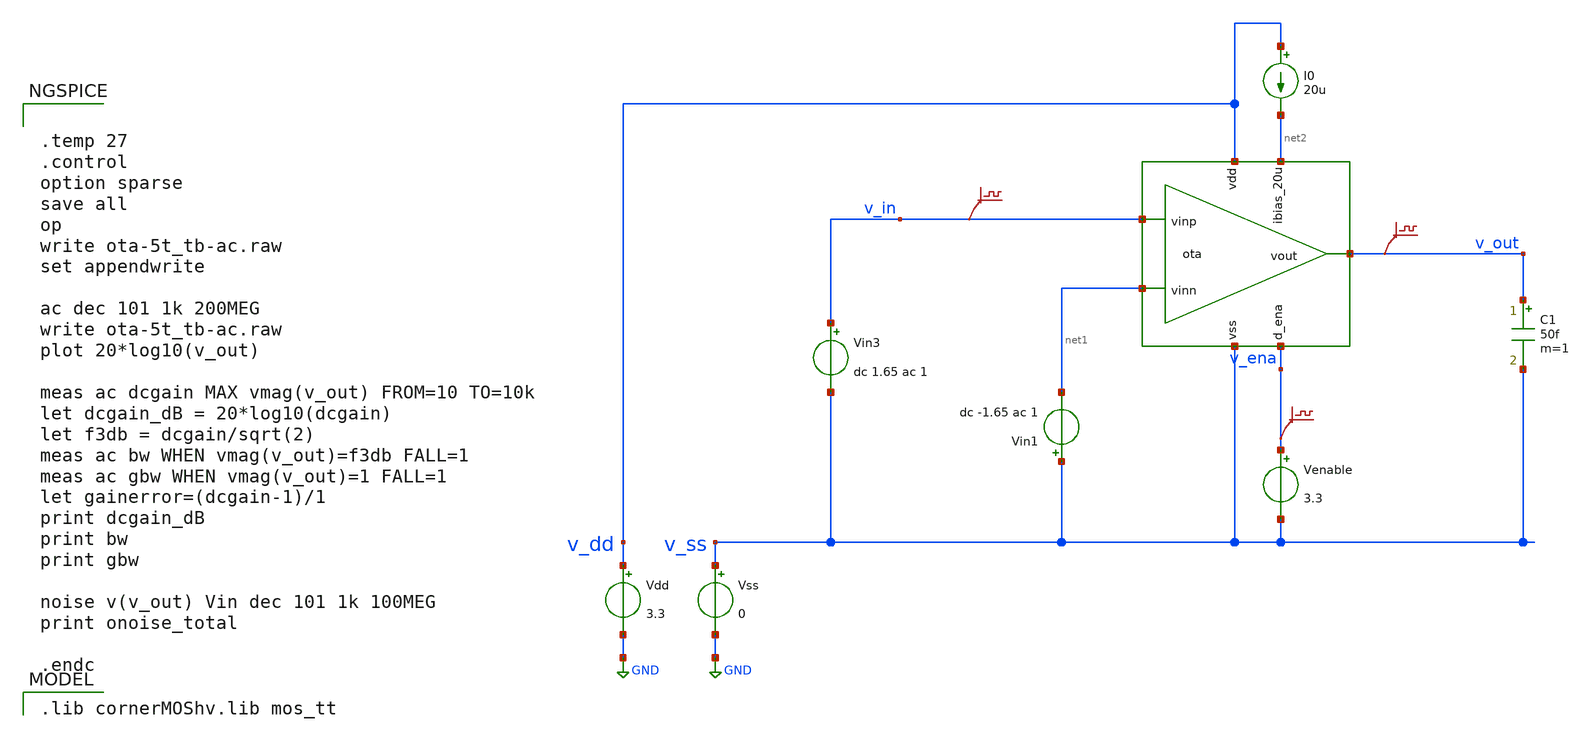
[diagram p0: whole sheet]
** sch_path: Differntial_Amp/design_data/xschem/ota-5t_tb-ac.sch
* Copyright 2024 Harald Pretl
**.subckt ota-5t_tb-ac
Vdd v_dd GND 3.3
Vss v_ss GND 0
C1 v_out v_ss 50f m=1
I0 v_dd net2 20u
Venable v_ena v_ss 3.3
.save v(v_in)
.save v(v_out)
.save v(v_ena)
x1 v_dd v_out v_in net1 net2 v_ss v_ena ota
Vin1 v_ss net1 dc -1.65 ac 1
Vin3 v_in v_ss dc 1.65 ac 1
**** begin user architecture code
 .lib cornerMOShv.lib mos_tt



.temp 27
.control
option sparse
save all
op
write ota-5t_tb-ac.raw
set appendwrite

ac dec 101 1k 200MEG
write ota-5t_tb-ac.raw
plot 20*log10(v_out)

meas ac dcgain MAX vmag(v_out) FROM=10 TO=10k
let dcgain_dB = 20*log10(dcgain)
let f3db = dcgain/sqrt(2)
meas ac bw WHEN vmag(v_out)=f3db FALL=1
meas ac gbw WHEN vmag(v_out)=1 FALL=1
let gainerror=(dcgain-1)/1
print dcgain_dB
print bw
print gbw

noise v(v_out) Vin dec 101 1k 100MEG
print onoise_total

.endc


**** end user architecture code
**.ends

* expanding   symbol:
*+  /home/aidas93/Downloads/TO_Nov2024-main/Differntial_Amp/design_data/xschem/ota.sym # of pins=7
** sym_path: Differntial_Amp/design_data/xschem/ota.sym
** sch_path: Differntial_Amp/design_data/xschem/ota.sch
.subckt ota vdd vout vinp vinn ibias_20u vss d_ena
*.opin vout
*.iopin vdd
*.iopin vss
*.ipin ibias_20u
*.ipin vinn
*.ipin vinp
*.ipin d_ena
XM1 vout vinn net2 vss sg13_hv_nmos w=0.53u l=1u ng=1 m=4 mm_ok=1
XM2 net1 vinp net2 vss sg13_hv_nmos w=0.53u l=1u ng=1 m=4 mm_ok=1
XM5 net2 net3 vss vss sg13_hv_nmos w=0.76u l=1u ng=1 m=1 mm_ok=1
XM3 net1 net1 vdd vdd sg13_hv_pmos w=1.45u l=1u ng=1 m=1 mm_ok=1
XM4 vout net1 vdd vdd sg13_hv_pmos w=1.45u l=1u ng=1 m=1 mm_ok=1
XM6 ibias_20u net3 vss vss sg13_hv_nmos w=3.075u l=1u ng=5 m=1 mm_ok=1
XM7 net1 d_ena vdd vdd sg13_hv_pmos w=1.5u l=1u ng=1 m=1 mm_ok=1
XM8 net4 d_ena vdd vdd sg13_hv_pmos w=1.5u l=1u ng=1 m=1 mm_ok=1
XM9 ibias_20u net4 net3 vss sg13_hv_nmos w=0.5u l=1u ng=1 m=1 mm_ok=1
XM10 net3 net4 vss vss sg13_hv_nmos w=0.5u l=1u ng=1 m=1 mm_ok=1
XM11 net4 d_ena vss vss sg13_hv_nmos w=0.5u l=1u ng=1 m=1 mm_ok=1
XM12 vss vss vss vss sg13_hv_nmos w=0.5u l=0.5u ng=1 m=1 mm_ok=1
XM13 vss vss vss vss sg13_hv_nmos w=0.5u l=0.5u ng=1 m=1 mm_ok=1
XM14 vss vss vss vss sg13_hv_nmos w=0.76u l=0.5u ng=1 m=1 mm_ok=1
XM15 vss vss vss vss sg13_hv_nmos w=0.615u l=0.5u ng=1 m=1 mm_ok=1
XM16 vss vss vss vss sg13_hv_nmos w=0.615u l=0.5u ng=1 m=1 mm_ok=1
XM17 vss vss vss vss sg13_hv_nmos w=0.76u l=0.5u ng=1 m=1 mm_ok=1
XM18 vss vss vss vss sg13_hv_nmos w=0.5u l=0.5u ng=1 m=1 mm_ok=1
XM19 vss vss vss vss sg13_hv_nmos w=0.5u l=0.5u ng=1 m=1 mm_ok=1
XM20 vss vss vss vss sg13_hv_nmos w=0.53u l=0.5u ng=1 m=1 mm_ok=1
XM21 vss vss vss vss sg13_hv_nmos w=0.53u l=0.5u ng=1 m=1 mm_ok=1
XM22 vss vss vss vss sg13_hv_nmos w=0.53u l=0.5u ng=1 m=1 mm_ok=1
XM23 vss vss vss vss sg13_hv_nmos w=0.53u l=0.5u ng=1 m=1 mm_ok=1
XM24 vss vss vss vss sg13_hv_nmos w=0.5u l=1u ng=1 m=1 mm_ok=1
XM25 vss vss vss vss sg13_hv_nmos w=0.5u l=1u ng=1 m=1 mm_ok=1
XM26 vss vss vss vss sg13_hv_nmos w=0.5u l=0.5u ng=1 m=1 mm_ok=1
XM27 vss vss vss vss sg13_hv_nmos w=0.5u l=0.5u ng=1 m=1 mm_ok=1
XM28 vss vss vss vss sg13_hv_nmos w=0.53u l=0.5u ng=1 m=1 mm_ok=1
XM29 vss vss vss vss sg13_hv_nmos w=0.53u l=0.5u ng=1 m=1 mm_ok=1
XM30 vss vss vss vss sg13_hv_nmos w=0.53u l=0.5u ng=1 m=1 mm_ok=1
XM31 vss vss vss vss sg13_hv_nmos w=0.53u l=0.5u ng=1 m=1 mm_ok=1
XM32 vss vss vss vss sg13_hv_nmos w=0.5u l=1u ng=1 m=1 mm_ok=1
XM33 vss vss vss vss sg13_hv_nmos w=0.5u l=1u ng=1 m=1 mm_ok=1
XM34 vdd vdd vdd vdd sg13_hv_pmos w=1.45u l=0.5u ng=1 m=1 mm_ok=1
XM35 vdd vdd vdd vdd sg13_hv_pmos w=1.45u l=0.5u ng=1 m=1 mm_ok=1
XM36 vdd vdd vdd vdd sg13_hv_pmos w=1.45u l=0.5u ng=1 m=1 mm_ok=1
XM37 vdd vdd vdd vdd sg13_hv_pmos w=1.45u l=0.5u ng=1 m=1 mm_ok=1
.ends

.GLOBAL GND
.end
